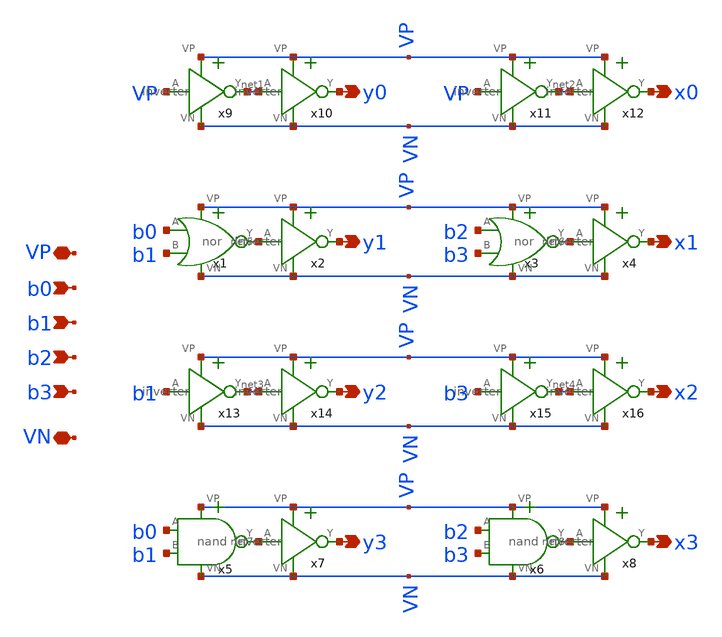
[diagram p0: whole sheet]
** sch_path: xschem/binary_decoder_4bit.sch
**.subckt binary_decoder_4bit b0 b1 b2 b3 x0 x1 x2 x3 y0 y1 y2 y3 VP VN
*.ipin b0
*.ipin b1
*.ipin b2
*.ipin b3
*.opin x0
*.opin x1
*.opin x2
*.opin x3
*.opin y0
*.opin y1
*.opin y2
*.opin y3
*.iopin VP
*.iopin VN
x1 VN b0 b1 net5 VP nor
x2 VP net5 y1 VN inverter
x3 VN b2 b3 net6 VP nor
x4 VP net6 x1 VN inverter
x5 VN b0 b1 net7 VP nand
x6 VN b2 b3 net8 VP nand
x7 VP net7 y3 VN inverter
x8 VP net8 x3 VN inverter
x9 VP VP net1 VN inverter
x10 VP net1 y0 VN inverter
x11 VP VP net2 VN inverter
x12 VP net2 x0 VN inverter
x13 VP b1 net3 VN inverter
x14 VP net3 y2 VN inverter
x15 VP b3 net4 VN inverter
x16 VP net4 x2 VN inverter
**.ends

* expanding   symbol:  /home/madvlsi/dev/git/magic-dds/xschem/logic_gates/nor.sym # of pins=5
** sym_path: xschem/logic_gates/nor.sym
** sch_path: xschem/logic_gates/nor.sch
.subckt nor VN A B Y VP
*.iopin VP
*.iopin VN
*.ipin A
*.ipin B
*.opin Y
XM1 Y A VN GND sky130_fd_pr__nfet_01v8 L=0.15 W=1 nf=1 ad='int((nf+1)/2) * W/nf * 0.29' as='int((nf+2)/2) * W/nf * 0.29'
+ pd='2*int((nf+1)/2) * (W/nf + 0.29)' ps='2*int((nf+2)/2) * (W/nf + 0.29)' nrd='0.29 / W' nrs='0.29 / W'
+ sa=0 sb=0 sd=0 mult=1 m=1
XM2 Y B VN GND sky130_fd_pr__nfet_01v8 L=0.15 W=1 nf=1 ad='int((nf+1)/2) * W/nf * 0.29' as='int((nf+2)/2) * W/nf * 0.29'
+ pd='2*int((nf+1)/2) * (W/nf + 0.29)' ps='2*int((nf+2)/2) * (W/nf + 0.29)' nrd='0.29 / W' nrs='0.29 / W'
+ sa=0 sb=0 sd=0 mult=1 m=1
XM3 Y A net1 VDD sky130_fd_pr__pfet_01v8 L=0.15 W=1 nf=1 ad='int((nf+1)/2) * W/nf * 0.29' as='int((nf+2)/2) * W/nf * 0.29'
+ pd='2*int((nf+1)/2) * (W/nf + 0.29)' ps='2*int((nf+2)/2) * (W/nf + 0.29)' nrd='0.29 / W' nrs='0.29 / W'
+ sa=0 sb=0 sd=0 mult=1 m=1
XM4 net1 B VP VDD sky130_fd_pr__pfet_01v8 L=0.15 W=1 nf=1 ad='int((nf+1)/2) * W/nf * 0.29' as='int((nf+2)/2) * W/nf * 0.29'
+ pd='2*int((nf+1)/2) * (W/nf + 0.29)' ps='2*int((nf+2)/2) * (W/nf + 0.29)' nrd='0.29 / W' nrs='0.29 / W'
+ sa=0 sb=0 sd=0 mult=1 m=1
.ends


* expanding   symbol:  /home/madvlsi/dev/git/magic-dds/xschem/other_project_files/inverter.sym # of
*+ pins=4
** sym_path: xschem/other_project_files/inverter.sym
** sch_path: xschem/other_project_files/inverter.sch
.subckt inverter VP A Y VN
*.iopin VP
*.iopin VN
*.ipin A
*.opin Y
XM1 Y A VN VN sky130_fd_pr__nfet_01v8 L=0.15 W=1 nf=1 ad='int((nf+1)/2) * W/nf * 0.29' as='int((nf+2)/2) * W/nf * 0.29'
+ pd='2*int((nf+1)/2) * (W/nf + 0.29)' ps='2*int((nf+2)/2) * (W/nf + 0.29)' nrd='0.29 / W' nrs='0.29 / W'
+ sa=0 sb=0 sd=0 mult=1 m=1
XM2 Y A VP VP sky130_fd_pr__pfet_01v8 L=0.15 W=4 nf=1 ad='int((nf+1)/2) * W/nf * 0.29' as='int((nf+2)/2) * W/nf * 0.29'
+ pd='2*int((nf+1)/2) * (W/nf + 0.29)' ps='2*int((nf+2)/2) * (W/nf + 0.29)' nrd='0.29 / W' nrs='0.29 / W'
+ sa=0 sb=0 sd=0 mult=1 m=1
.ends


* expanding   symbol:  /home/madvlsi/dev/git/magic-dds/xschem/logic_gates/nand.sym # of pins=5
** sym_path: xschem/logic_gates/nand.sym
** sch_path: xschem/logic_gates/nand.sch
.subckt nand VN A B Y VP
*.iopin VP
*.iopin VN
*.ipin A
*.ipin B
*.opin Y
XM1 Y A net1 GND sky130_fd_pr__nfet_01v8 L=0.15 W=1 nf=1 ad='int((nf+1)/2) * W/nf * 0.29' as='int((nf+2)/2) * W/nf * 0.29'
+ pd='2*int((nf+1)/2) * (W/nf + 0.29)' ps='2*int((nf+2)/2) * (W/nf + 0.29)' nrd='0.29 / W' nrs='0.29 / W'
+ sa=0 sb=0 sd=0 mult=1 m=1
XM2 net1 B VN GND sky130_fd_pr__nfet_01v8 L=0.15 W=1 nf=1 ad='int((nf+1)/2) * W/nf * 0.29' as='int((nf+2)/2) * W/nf * 0.29'
+ pd='2*int((nf+1)/2) * (W/nf + 0.29)' ps='2*int((nf+2)/2) * (W/nf + 0.29)' nrd='0.29 / W' nrs='0.29 / W'
+ sa=0 sb=0 sd=0 mult=1 m=1
XM3 Y A VP VDD sky130_fd_pr__pfet_01v8 L=0.15 W=1 nf=1 ad='int((nf+1)/2) * W/nf * 0.29' as='int((nf+2)/2) * W/nf * 0.29'
+ pd='2*int((nf+1)/2) * (W/nf + 0.29)' ps='2*int((nf+2)/2) * (W/nf + 0.29)' nrd='0.29 / W' nrs='0.29 / W'
+ sa=0 sb=0 sd=0 mult=1 m=1
XM4 Y B VP VDD sky130_fd_pr__pfet_01v8 L=0.15 W=1 nf=1 ad='int((nf+1)/2) * W/nf * 0.29' as='int((nf+2)/2) * W/nf * 0.29'
+ pd='2*int((nf+1)/2) * (W/nf + 0.29)' ps='2*int((nf+2)/2) * (W/nf + 0.29)' nrd='0.29 / W' nrs='0.29 / W'
+ sa=0 sb=0 sd=0 mult=1 m=1
.ends

.end
